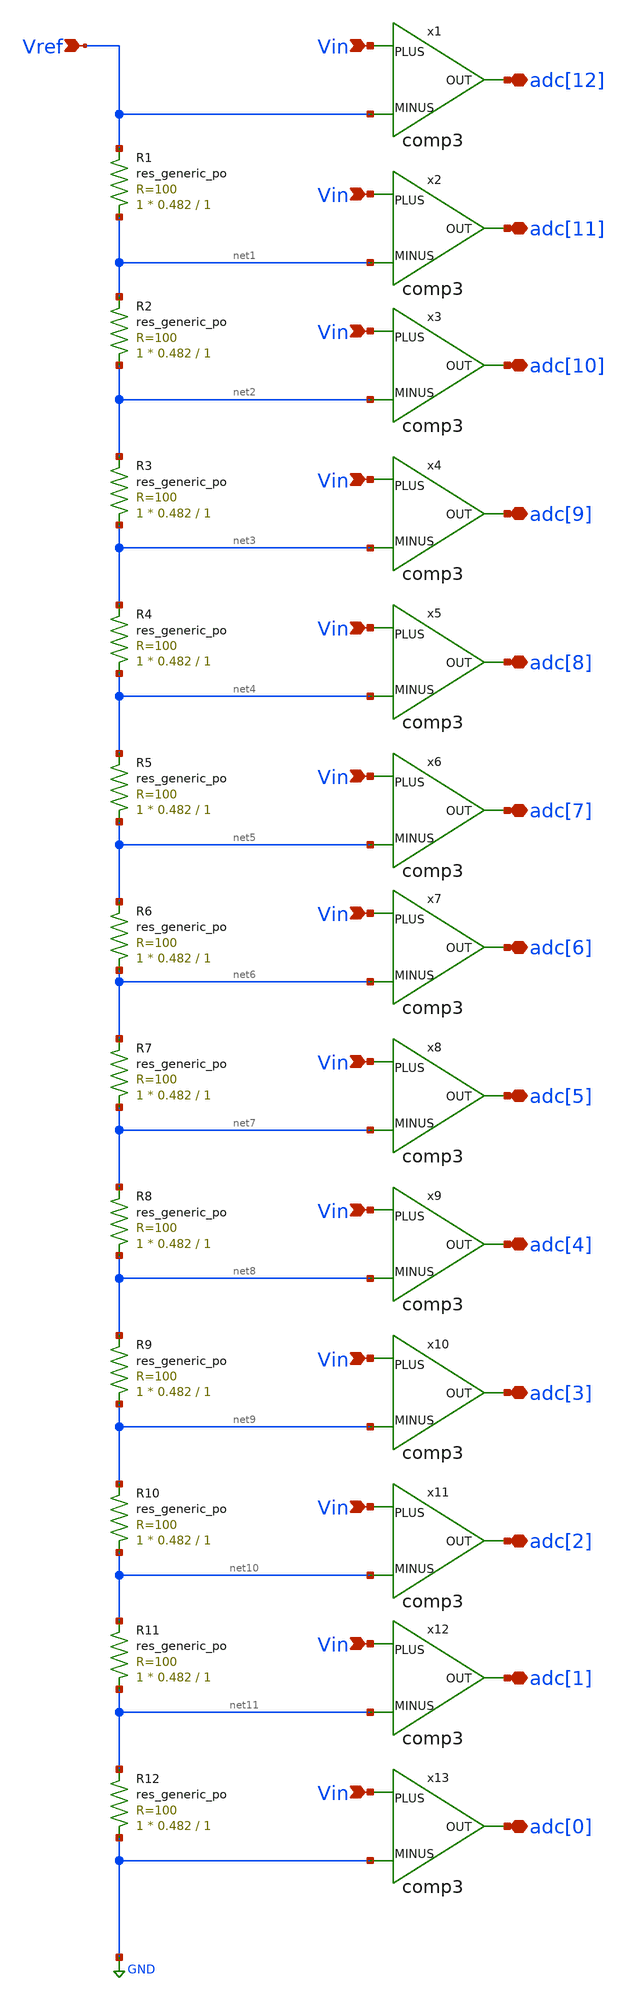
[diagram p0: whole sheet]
** sch_path: xschem/analog_desing/ADC/ADC.sch
* StefanSchippers/xschem/xschem_library/inst_sch_select/comp3.sch:
* Copyright (C) 1998-2024 Stefan Frederik Schippers
* This program is free software; you can redistribute it and/or modify
* it under the terms of the GNU General Public License as published by
* the Free Software Foundation; either version 2 of the License, or
* (at your option) any later version.
**.subckt ADC Vin adc[12] Vin adc[11] Vin adc[10] Vin adc[9] Vin adc[8] Vin adc[7] Vin adc[6] Vin
*+ adc[5] Vin adc[4] Vin adc[3] Vin adc[2] Vin adc[1] Vin adc[0] Vref
*.ipin Vin
*.iopin adc[12]
*.ipin Vin
*.iopin adc[11]
*.ipin Vin
*.iopin adc[10]
*.ipin Vin
*.iopin adc[9]
*.ipin Vin
*.iopin adc[8]
*.ipin Vin
*.iopin adc[7]
*.ipin Vin
*.iopin adc[6]
*.ipin Vin
*.iopin adc[5]
*.ipin Vin
*.iopin adc[4]
*.ipin Vin
*.iopin adc[3]
*.ipin Vin
*.iopin adc[2]
*.ipin Vin
*.iopin adc[1]
*.ipin Vin
*.iopin adc[0]
*.ipin Vref
x1 Vin adc[12] Vref comp3
x2 Vin adc[11] net1 comp3
x3 Vin adc[10] net2 comp3
x4 Vin adc[9] net3 comp3
x5 Vin adc[8] net4 comp3
x6 Vin adc[7] net5 comp3
x7 Vin adc[6] net6 comp3
x8 Vin adc[5] net7 comp3
x9 Vin adc[4] net8 comp3
x10 Vin adc[3] net9 comp3
x11 Vin adc[2] net10 comp3
x12 Vin adc[1] net11 comp3
x13 Vin adc[0] GND comp3
XR1 net1 Vref sky130_fd_pr__res_generic_po W=0.482 L=1 m=1
XR2 net2 net1 sky130_fd_pr__res_generic_po W=0.482 L=1 m=1
XR3 net3 net2 sky130_fd_pr__res_generic_po W=0.482 L=1 m=1
XR4 net4 net3 sky130_fd_pr__res_generic_po W=0.482 L=1 m=1
XR5 net5 net4 sky130_fd_pr__res_generic_po W=0.482 L=1 m=1
XR6 net6 net5 sky130_fd_pr__res_generic_po W=0.482 L=1 m=1
XR7 net7 net6 sky130_fd_pr__res_generic_po W=0.482 L=1 m=1
XR8 net8 net7 sky130_fd_pr__res_generic_po W=0.482 L=1 m=1
XR9 net9 net8 sky130_fd_pr__res_generic_po W=0.482 L=1 m=1
XR10 net10 net9 sky130_fd_pr__res_generic_po W=0.482 L=1 m=1
XR11 net11 net10 sky130_fd_pr__res_generic_po W=0.482 L=1 m=1
XR12 GND net11 sky130_fd_pr__res_generic_po W=0.482 L=1 m=1
**.ends

* expanding   symbol:  comp3.sym # of pins=3
** sym_path: comp3.sym
** sch_path: comp3.sch
.subckt comp3 PLUS OUT MINUS
*.ipin PLUS
*.ipin MINUS
*.opin OUT
M1 net1 GN1 0 0 nmos w=4u l=0.4u m=1
M2 GN1 GN1 0 0 nmos w=4u l=0.4u m=1
I0 VCC GN1 30u
M3 net2 MINUS net1 0 nmos w=1.5u l=0.2u m=1
M4 net3 PLUS net1 0 nmos w=1.5u l=0.2u m=1
M5 net2 net2 VCC VCC pmos w=6u l=0.3u m=1
M6 net3 net2 VCC VCC pmos w=6u l=0.3u m=1
M14 net4 net3 VCC VCC pmos w=6u l=0.3u m=1
.save v(gn1)
.save v(net2)
M7 net4 GN1 0 0 nmos w=4u l=0.4u m=1
M8 net5 net4 0 0 nmos w=1u l=0.4u m=1
M9 net5 net4 VCC VCC pmos w=2u l=0.4u m=1
M10 OUT net5 0 0 nmos w=1u l=0.4u m=1
M11 OUT net5 VCC VCC pmos w=2u l=0.4u m=1
M13 net4 net4 net5 0 nmos w=2u l=0.1u m=1
.save v(net5)
.save v(net4)
M12 net5 net5 net4 0 nmos w=2u l=0.1u m=1
.save v(net1)
C2 GN1 0 200f m=1
.ends

.GLOBAL GND
.GLOBAL VCC
.end
